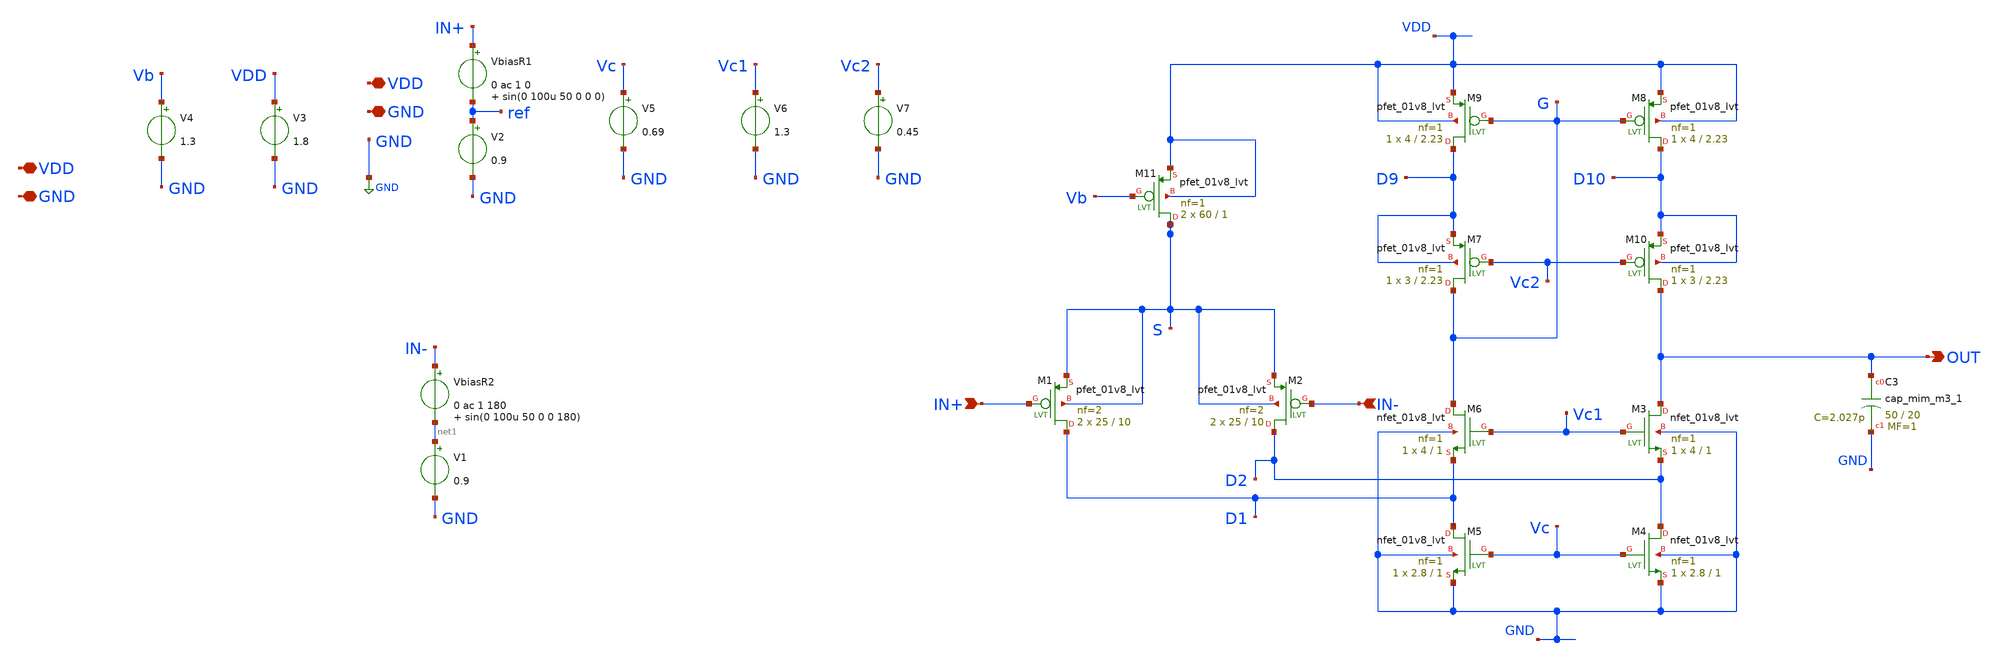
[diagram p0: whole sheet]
** sch_path: xschem/OTA_FoldedCascode_AC1.sch
**.subckt OTA_FoldedCascode_AC1 VDD GND VDD GND OUT IN+ IN-
*.iopin VDD
*.iopin GND
*.iopin VDD
*.iopin GND
*.opin OUT
*.ipin IN+
*.ipin IN-
VbiasR1 IN+ ref 0 ac 1 0 sin(0 100u 50 0 0 0)
V2 ref GND 0.9
V3 VDD GND 1.8
V4 Vb GND 1.3
V5 Vc GND 0.69
V6 Vc1 GND 1.3
V7 Vc2 GND 0.45
XC3 OUT GND sky130_fd_pr__cap_mim_m3_1 W=50 L=20 MF=1 m=1
XM11 S Vb VDD VDD sky130_fd_pr__pfet_01v8_lvt L=1 W=60 nf=1 ad='int((nf+1)/2) * W/nf * 0.29' as='int((nf+2)/2) * W/nf * 0.29'
+ pd='2*int((nf+1)/2) * (W/nf + 0.29)' ps='2*int((nf+2)/2) * (W/nf + 0.29)' nrd='0.29 / W' nrs='0.29 / W'
+ sa=0 sb=0 sd=0 mult=2 m=2
XM1 D1 IN+ S S sky130_fd_pr__pfet_01v8_lvt L=10 W=25 nf=2 ad='int((nf+1)/2) * W/nf * 0.29' as='int((nf+2)/2) * W/nf * 0.29'
+ pd='2*int((nf+1)/2) * (W/nf + 0.29)' ps='2*int((nf+2)/2) * (W/nf + 0.29)' nrd='0.29 / W' nrs='0.29 / W'
+ sa=0 sb=0 sd=0 mult=2 m=2
XM2 D2 IN- S S sky130_fd_pr__pfet_01v8_lvt L=10 W=25 nf=2 ad='int((nf+1)/2) * W/nf * 0.29' as='int((nf+2)/2) * W/nf * 0.29'
+ pd='2*int((nf+1)/2) * (W/nf + 0.29)' ps='2*int((nf+2)/2) * (W/nf + 0.29)' nrd='0.29 / W' nrs='0.29 / W'
+ sa=0 sb=0 sd=0 mult=2 m=2
XM3 OUT Vc1 D2 GND sky130_fd_pr__nfet_01v8_lvt L=1 W=4 nf=1 ad='int((nf+1)/2) * W/nf * 0.29' as='int((nf+2)/2) * W/nf * 0.29'
+ pd='2*int((nf+1)/2) * (W/nf + 0.29)' ps='2*int((nf+2)/2) * (W/nf + 0.29)' nrd='0.29 / W' nrs='0.29 / W'
+ sa=0 sb=0 sd=0 mult=1 m=1
XM4 D2 Vc GND GND sky130_fd_pr__nfet_01v8_lvt L=1 W=2.8 nf=1 ad='int((nf+1)/2) * W/nf * 0.29' as='int((nf+2)/2) * W/nf * 0.29'
+ pd='2*int((nf+1)/2) * (W/nf + 0.29)' ps='2*int((nf+2)/2) * (W/nf + 0.29)' nrd='0.29 / W' nrs='0.29 / W'
+ sa=0 sb=0 sd=0 mult=1 m=1
XM5 D1 Vc GND GND sky130_fd_pr__nfet_01v8_lvt L=1 W=2.8 nf=1 ad='int((nf+1)/2) * W/nf * 0.29' as='int((nf+2)/2) * W/nf * 0.29'
+ pd='2*int((nf+1)/2) * (W/nf + 0.29)' ps='2*int((nf+2)/2) * (W/nf + 0.29)' nrd='0.29 / W' nrs='0.29 / W'
+ sa=0 sb=0 sd=0 mult=1 m=1
XM6 G Vc1 D1 GND sky130_fd_pr__nfet_01v8_lvt L=1 W=4 nf=1 ad='int((nf+1)/2) * W/nf * 0.29' as='int((nf+2)/2) * W/nf * 0.29'
+ pd='2*int((nf+1)/2) * (W/nf + 0.29)' ps='2*int((nf+2)/2) * (W/nf + 0.29)' nrd='0.29 / W' nrs='0.29 / W'
+ sa=0 sb=0 sd=0 mult=1 m=1
XM7 G Vc2 D9 D9 sky130_fd_pr__pfet_01v8_lvt L=2.23 W=3 nf=1 ad='int((nf+1)/2) * W/nf * 0.29' as='int((nf+2)/2) * W/nf * 0.29'
+ pd='2*int((nf+1)/2) * (W/nf + 0.29)' ps='2*int((nf+2)/2) * (W/nf + 0.29)' nrd='0.29 / W' nrs='0.29 / W'
+ sa=0 sb=0 sd=0 mult=1 m=1
XM9 D9 G VDD VDD sky130_fd_pr__pfet_01v8_lvt L=2.23 W=4 nf=1 ad='int((nf+1)/2) * W/nf * 0.29' as='int((nf+2)/2) * W/nf * 0.29'
+ pd='2*int((nf+1)/2) * (W/nf + 0.29)' ps='2*int((nf+2)/2) * (W/nf + 0.29)' nrd='0.29 / W' nrs='0.29 / W'
+ sa=0 sb=0 sd=0 mult=1 m=1
XM8 D10 G VDD VDD sky130_fd_pr__pfet_01v8_lvt L=2.23 W=4 nf=1 ad='int((nf+1)/2) * W/nf * 0.29' as='int((nf+2)/2) * W/nf * 0.29'
+ pd='2*int((nf+1)/2) * (W/nf + 0.29)' ps='2*int((nf+2)/2) * (W/nf + 0.29)' nrd='0.29 / W' nrs='0.29 / W'
+ sa=0 sb=0 sd=0 mult=1 m=1
XM10 OUT Vc2 D10 D10 sky130_fd_pr__pfet_01v8_lvt L=2.23 W=3 nf=1 ad='int((nf+1)/2) * W/nf * 0.29' as='int((nf+2)/2) * W/nf * 0.29'
+ pd='2*int((nf+1)/2) * (W/nf + 0.29)' ps='2*int((nf+2)/2) * (W/nf + 0.29)' nrd='0.29 / W' nrs='0.29 / W'
+ sa=0 sb=0 sd=0 mult=1 m=1
VbiasR2 IN- net1 0 ac 1 180 sin(0 100u 50 0 0 180)
V1 net1 GND 0.9
**** begin user architecture code



.option reltol=1e-5   abstol=1e-14 savecurrents
.control
  save all
  op
  remzerovec
  write OTA_FoldedCascode_AC1.raw

  set appendwrite
  ac dec 10 1 1e9
  remzerovec
  write OTA_FoldedCascode_AC1.raw

  tran 100u 100m
  write OTA_FoldedCascode_AC1.raw

.endc



.lib $::SKYWATER_MODELS/sky130.lib.spice tt
**** end user architecture code
**.ends
.GLOBAL GND
.end
